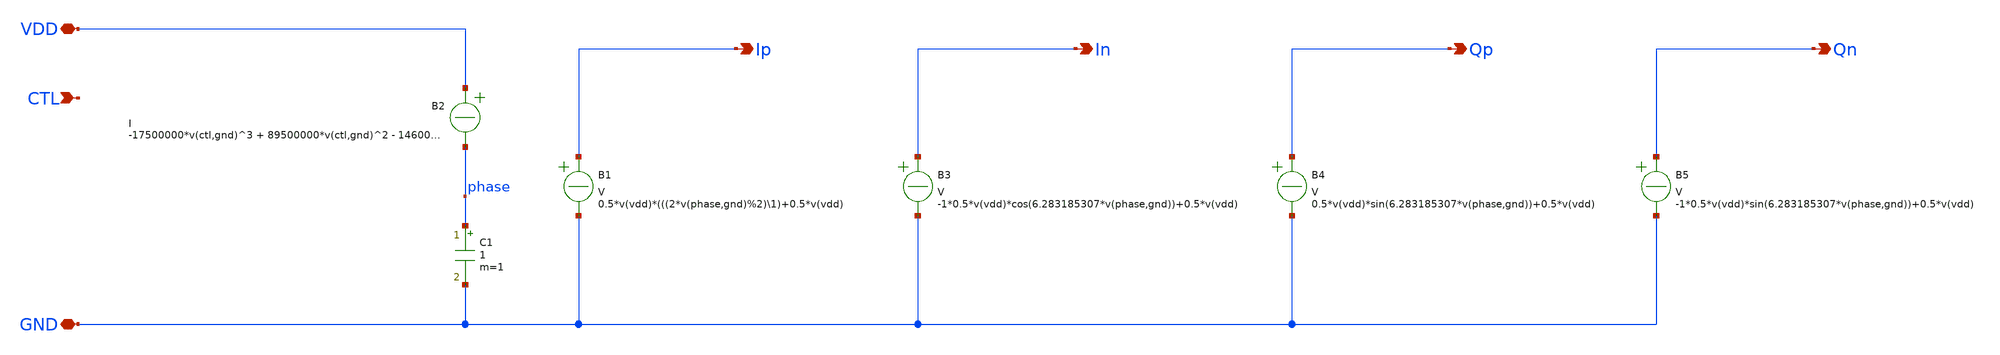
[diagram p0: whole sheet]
** sch_path: design/vco_2-4GHz/vco_2-4GHz_behavourial_square.sch
**.subckt vco_2-4GHz_behavourial_square CTL VDD GND Ip In Qp Qn
*.ipin CTL
*.iopin VDD
*.iopin GND
*.opin Ip
*.opin In
*.opin Qp
*.opin Qn
C1 phase GND 1 m=1
B2 VDD phase I = -17500000*v(ctl,gnd)^3 + 89500000*v(ctl,gnd)^2 - 146000000*v(ctl,gnd) + 181000000
B1 Ip GND V = 0.5*v(vdd)*(((2*v(phase,gnd)%2)\1)+0.5*v(vdd)
B3 In GND V = -1*0.5*v(vdd)*cos(6.283185307*v(phase,gnd))+0.5*v(vdd)
B4 Qp GND V = 0.5*v(vdd)*sin(6.283185307*v(phase,gnd))+0.5*v(vdd)
B5 Qn GND V = -1*0.5*v(vdd)*sin(6.283185307*v(phase,gnd))+0.5*v(vdd)
**.ends
.end
